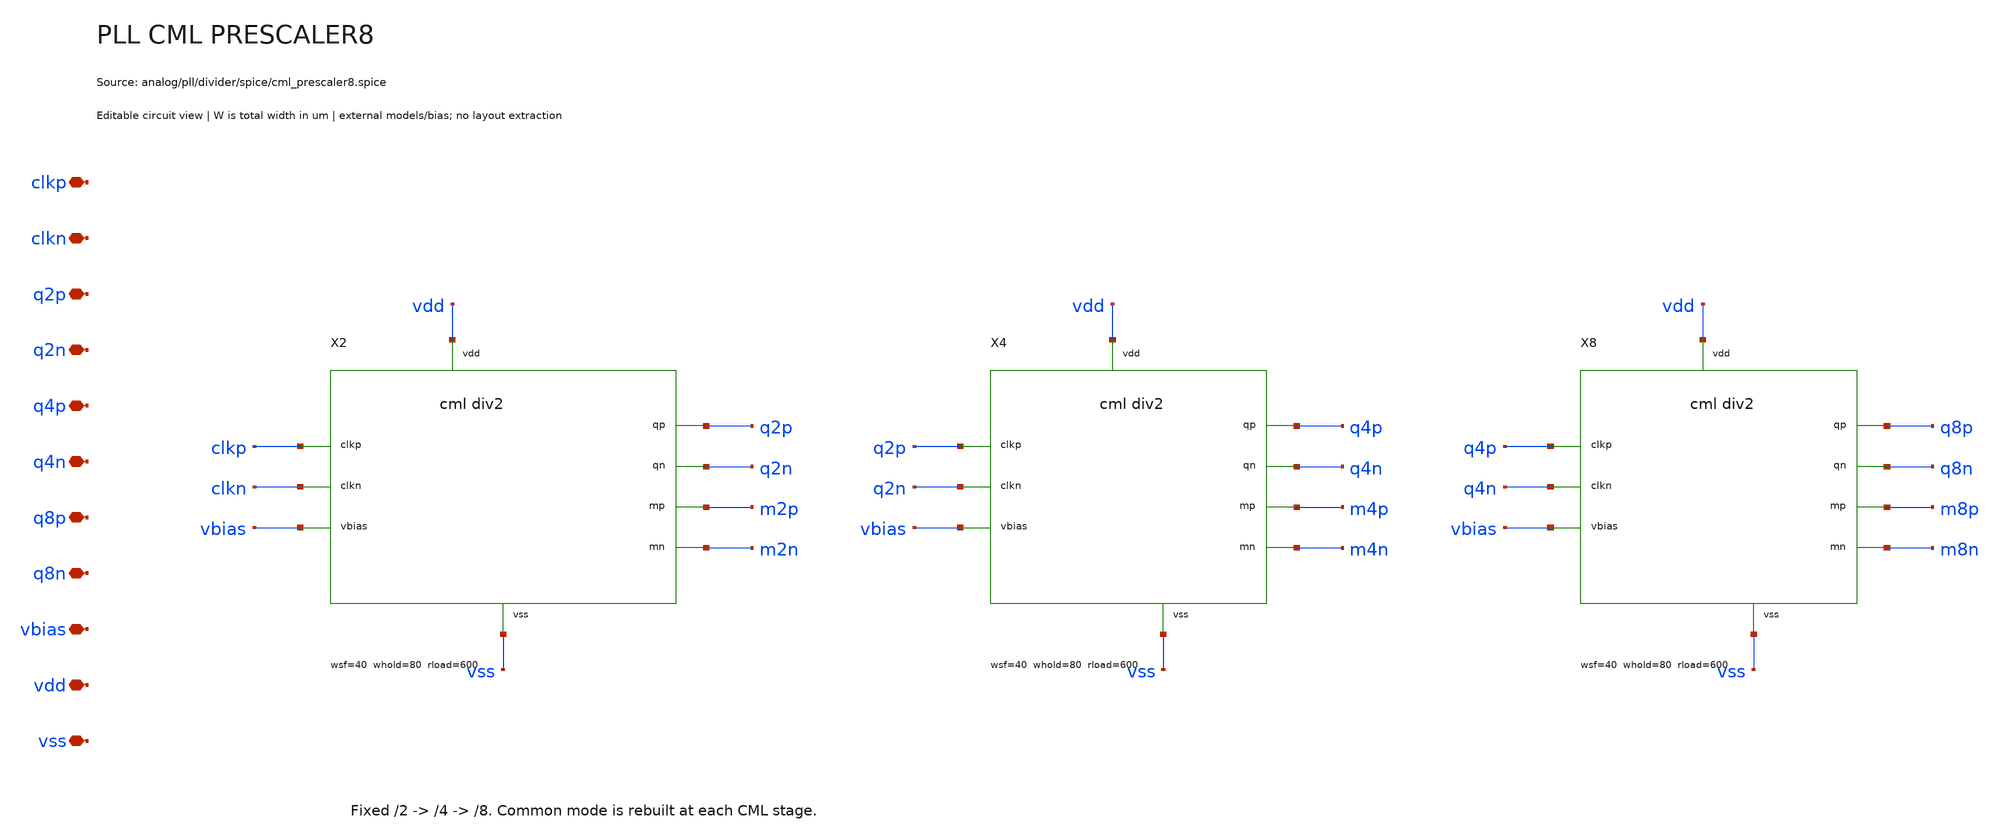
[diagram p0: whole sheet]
** sch_path: analog/pll/divider/schematic/pll_cml_prescaler8.sch
**.subckt pll_cml_prescaler8 clkp clkn q2p q2n q4p q4n q8p q8n vbias vdd vss
*.iopin clkp
*.iopin clkn
*.iopin q2p
*.iopin q2n
*.iopin q4p
*.iopin q4n
*.iopin q8p
*.iopin q8n
*.iopin vbias
*.iopin vdd
*.iopin vss
X2 clkp clkn q2p q2n m2p m2n vbias vdd vss pll_cml_div2 wsf=40 wsf_sink=4 wdata=20 whold=80
+ wclock=64 wtail=12 rload=600
X4 q2p q2n q4p q4n m4p m4n vbias vdd vss pll_cml_div2 wsf=40 wsf_sink=4 wdata=20 whold=80 wclock=64
+ wtail=12 rload=600
X8 q4p q4n q8p q8n m8p m8n vbias vdd vss pll_cml_div2 wsf=40 wsf_sink=4 wdata=20 whold=80 wclock=64
+ wtail=12 rload=600
**.ends

* expanding   symbol:  serdes/pll_cml_div2.sym # of pins=9
** sym_path: analog/pll/divider/schematic/pll_cml_div2.sym
** sch_path: analog/pll/divider/schematic/pll_cml_div2.sch
.subckt pll_cml_div2 clkp clkn qp qn mp mn vbias vdd vss  wsf=40 wsf_sink=4 wdata=20 whold=80
+ wclock=64 wtail=12 rload=600
*.iopin clkp
*.iopin clkn
*.iopin qp
*.iopin qn
*.iopin mp
*.iopin mn
*.iopin vbias
*.iopin vdd
*.iopin vss
Xfp vdd clkp ckp vss serdes_nfet_lvt w={wsf} l=0.15 nf=4
Xfn vdd clkn ckn vss serdes_nfet_lvt w={wsf} l=0.15 nf=4
Xsp ckp vbias vss vss serdes_nfet w={wsf_sink} l=0.5 nf=1
Xsn ckn vbias vss vss serdes_nfet w={wsf_sink} l=0.5 nf=1
Xmaster qn qp mp mn ckp ckn vbias vdd vss pll_cml_latch wdata={wdata} whold={whold} wclock={wclock} wtail={wtail}
+ rload={rload}
Xslave mp mn qp qn ckn ckp vbias vdd vss pll_cml_latch wdata={wdata} whold={whold} wclock={wclock} wtail={wtail}
+ rload={rload}
.ends


* expanding   symbol:  serdes/serdes_nfet_lvt.sym # of pins=4
** sym_path: analog/common/devices/schematic/serdes_nfet_lvt.sym
** sch_path: analog/common/devices/schematic/serdes_nfet_lvt.sch
.subckt serdes_nfet_lvt d g s b  w=1 l=0.15 nf=1
*.iopin d
*.iopin g
*.iopin s
*.iopin b
Xmos d g s b sky130_fd_pr__nfet_01v8_lvt w={w} l={l} nf={nf} ad={floor((nf+1)/2)*(w/nf)*0.29} as={floor((nf+2)/2)*(w/nf)*0.29}
+ pd={2*floor((nf+1)/2)*(w/nf+0.29)} ps={2*floor((nf+2)/2)*(w/nf+0.29)}
.ends


* expanding   symbol:  serdes/serdes_nfet.sym # of pins=4
** sym_path: analog/common/devices/schematic/serdes_nfet.sym
** sch_path: analog/common/devices/schematic/serdes_nfet.sch
.subckt serdes_nfet d g s b  w=1 l=0.15 nf=1
*.iopin d
*.iopin g
*.iopin s
*.iopin b
Xmos d g s b sky130_fd_pr__nfet_01v8 w={w} l={l} nf={nf} ad={floor((nf+1)/2)*(w/nf)*0.29} as={floor((nf+2)/2)*(w/nf)*0.29}
+ pd={2*floor((nf+1)/2)*(w/nf+0.29)} ps={2*floor((nf+2)/2)*(w/nf+0.29)}
.ends


* expanding   symbol:  serdes/pll_cml_latch.sym # of pins=9
** sym_path: analog/pll/divider/schematic/pll_cml_latch.sym
** sch_path: analog/pll/divider/schematic/pll_cml_latch.sch
.subckt pll_cml_latch dp dn qp qn clk_track clk_hold vbias vdd vss  wdata=20 whold=20 wclock=24
+ wtail=12 rload=600
*.iopin dp
*.iopin dn
*.iopin qp
*.iopin qn
*.iopin clk_track
*.iopin clk_hold
*.iopin vbias
*.iopin vdd
*.iopin vss
Rp vdd qp {rload}
Rn vdd qn {rload}
Xdp qn dp track vss serdes_nfet_lvt w={wdata} l=0.15 nf=4
Xdn qp dn track vss serdes_nfet_lvt w={wdata} l=0.15 nf=4
Xhp qn qp hold vss serdes_nfet_lvt w={whold} l=0.15 nf=4
Xhn qp qn hold vss serdes_nfet_lvt w={whold} l=0.15 nf=4
Xct track clk_track tail vss serdes_nfet_lvt w={wclock} l=0.15 nf=4
Xch hold clk_hold tail vss serdes_nfet_lvt w={wclock} l=0.15 nf=4
Xtail tail vbias vss vss serdes_nfet w={wtail} l=0.5 nf=4
.ends

.end
